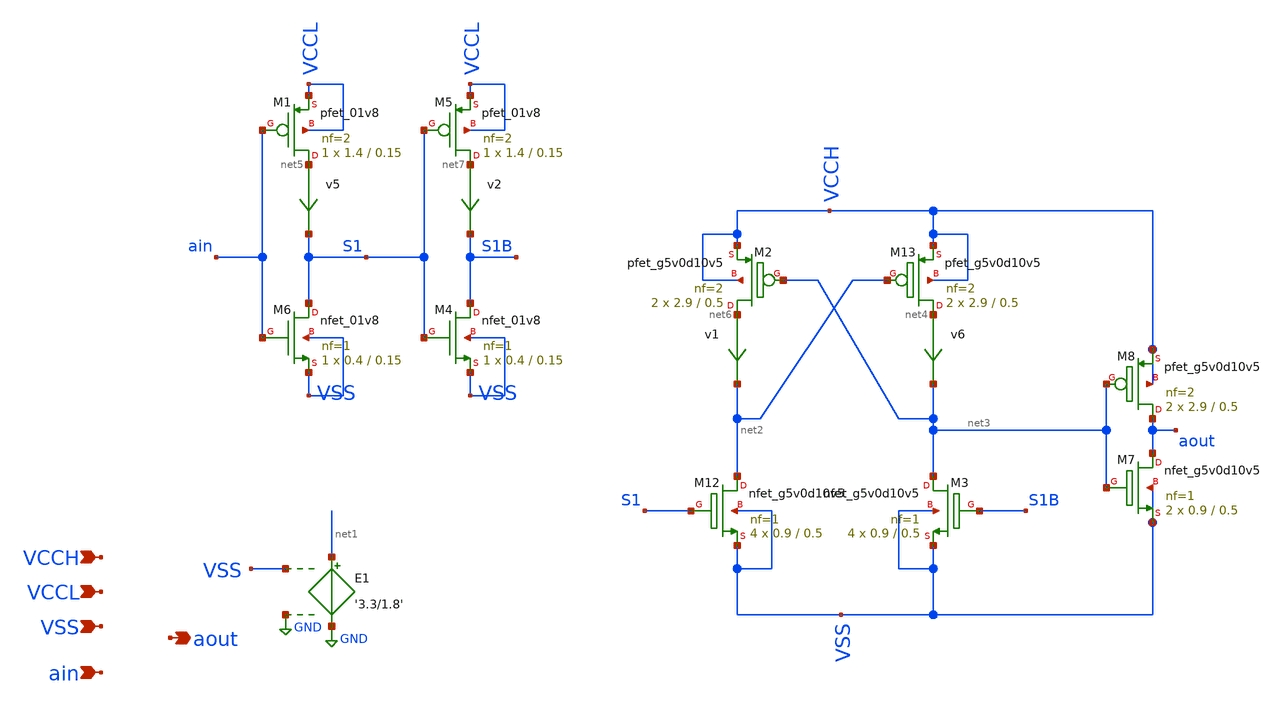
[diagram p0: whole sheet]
** sch_path: xschem/levelShifter.sch
**.subckt levelShifter VCCL VSS ain aout VCCH
*.ipin VCCL
*.ipin VSS
*.ipin ain
*.opin aout
*.ipin VCCH
E1 net1 GND VSS GND '3.3/1.8'
v6 net4 net3 0
.save i(v6)
XM12 net2 S1 VSS VSS sky130_fd_pr__nfet_g5v0d10v5 L=0.5 W=0.9 nf=1 ad='int((nf+1)/2) * W/nf * 0.29' as='int((nf+2)/2) * W/nf * 0.29'
+ pd='2*int((nf+1)/2) * (W/nf + 0.29)' ps='2*int((nf+2)/2) * (W/nf + 0.29)' nrd='0.29 / W' nrs='0.29 / W'
+ sa=0 sb=0 sd=0 mult=4 m=4
XM13 net4 net2 VCCH VCCH sky130_fd_pr__pfet_g5v0d10v5 L=0.5 W=2.9 nf=2 ad='int((nf+1)/2) * W/nf * 0.29'
+ as='int((nf+2)/2) * W/nf * 0.29' pd='2*int((nf+1)/2) * (W/nf + 0.29)' ps='2*int((nf+2)/2) * (W/nf + 0.29)'
+ nrd='0.29 / W' nrs='0.29 / W' sa=0 sb=0 sd=0 mult=2 m=2
v5 net5 S1 0
.save i(v5)
XM6 S1 ain VSS VSS sky130_fd_pr__nfet_01v8 L=0.15 W=0.4 nf=1 ad='int((nf+1)/2) * W/nf * 0.29' as='int((nf+2)/2) * W/nf * 0.29'
+ pd='2*int((nf+1)/2) * (W/nf + 0.29)' ps='2*int((nf+2)/2) * (W/nf + 0.29)' nrd='0.29 / W' nrs='0.29 / W'
+ sa=0 sb=0 sd=0 mult=1 m=1
XM1 net5 ain VCCL VCCL sky130_fd_pr__pfet_01v8 L=0.15 W=1.4 nf=2 ad='int((nf+1)/2) * W/nf * 0.29' as='int((nf+2)/2) * W/nf * 0.29'
+ pd='2*int((nf+1)/2) * (W/nf + 0.29)' ps='2*int((nf+2)/2) * (W/nf + 0.29)' nrd='0.29 / W' nrs='0.29 / W'
+ sa=0 sb=0 sd=0 mult=1 m=1
v1 net6 net2 0
.save i(v1)
XM2 net6 net3 VCCH VCCH sky130_fd_pr__pfet_g5v0d10v5 L=0.5 W=2.9 nf=2 ad='int((nf+1)/2) * W/nf * 0.29'
+ as='int((nf+2)/2) * W/nf * 0.29' pd='2*int((nf+1)/2) * (W/nf + 0.29)' ps='2*int((nf+2)/2) * (W/nf + 0.29)'
+ nrd='0.29 / W' nrs='0.29 / W' sa=0 sb=0 sd=0 mult=2 m=2
XM3 net3 S1B VSS VSS sky130_fd_pr__nfet_g5v0d10v5 L=0.5 W=0.9 nf=1 ad='int((nf+1)/2) * W/nf * 0.29' as='int((nf+2)/2) * W/nf * 0.29'
+ pd='2*int((nf+1)/2) * (W/nf + 0.29)' ps='2*int((nf+2)/2) * (W/nf + 0.29)' nrd='0.29 / W' nrs='0.29 / W'
+ sa=0 sb=0 sd=0 mult=4 m=4
v2 net7 S1B 0
.save i(v2)
XM4 S1B S1 VSS VSS sky130_fd_pr__nfet_01v8 L=0.15 W=0.4 nf=1 ad='int((nf+1)/2) * W/nf * 0.29' as='int((nf+2)/2) * W/nf * 0.29'
+ pd='2*int((nf+1)/2) * (W/nf + 0.29)' ps='2*int((nf+2)/2) * (W/nf + 0.29)' nrd='0.29 / W' nrs='0.29 / W'
+ sa=0 sb=0 sd=0 mult=1 m=1
XM5 net7 S1 VCCL VCCL sky130_fd_pr__pfet_01v8 L=0.15 W=1.4 nf=2 ad='int((nf+1)/2) * W/nf * 0.29' as='int((nf+2)/2) * W/nf * 0.29'
+ pd='2*int((nf+1)/2) * (W/nf + 0.29)' ps='2*int((nf+2)/2) * (W/nf + 0.29)' nrd='0.29 / W' nrs='0.29 / W'
+ sa=0 sb=0 sd=0 mult=1 m=1
XM7 aout net3 VSS VSS sky130_fd_pr__nfet_g5v0d10v5 L=0.5 W=0.9 nf=1 ad='int((nf+1)/2) * W/nf * 0.29'
+ as='int((nf+2)/2) * W/nf * 0.29' pd='2*int((nf+1)/2) * (W/nf + 0.29)' ps='2*int((nf+2)/2) * (W/nf + 0.29)'
+ nrd='0.29 / W' nrs='0.29 / W' sa=0 sb=0 sd=0 mult=2 m=2
XM8 aout net3 VCCH VCCH sky130_fd_pr__pfet_g5v0d10v5 L=0.5 W=2.9 nf=2 ad='int((nf+1)/2) * W/nf * 0.29'
+ as='int((nf+2)/2) * W/nf * 0.29' pd='2*int((nf+1)/2) * (W/nf + 0.29)' ps='2*int((nf+2)/2) * (W/nf + 0.29)'
+ nrd='0.29 / W' nrs='0.29 / W' sa=0 sb=0 sd=0 mult=2 m=2
**.ends
.GLOBAL GND
.end
